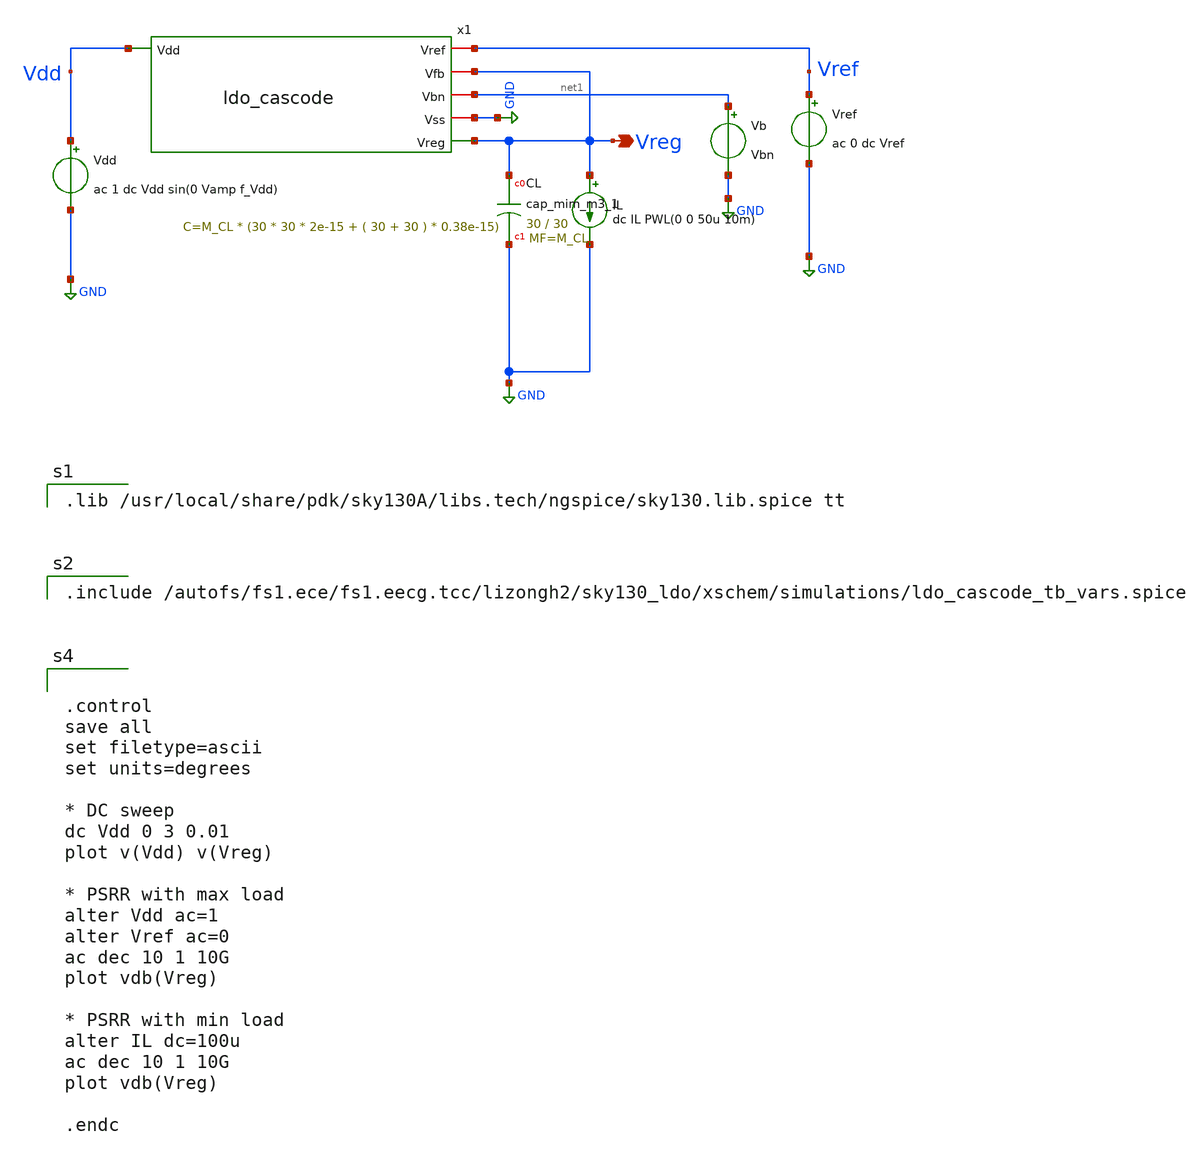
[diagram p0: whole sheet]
** sch_path: xschem/ldo_cascode_tb.sch
**.subckt ldo_cascode_tb Vreg
*.opin Vreg
Vref Vref GND ac 0 dc Vref
Vb net1 GND Vbn
IL Vreg GND dc IL PWL(0 0 50u 10m)
Vdd Vdd GND ac 1 dc Vdd sin(0 Vamp f_Vdd)
XCL Vreg GND sky130_fd_pr__cap_mim_m3_1 W=30 L=30 MF=M_CL m=M_CL
x1 Vdd Vref Vreg net1 GND Vreg ldo_cascode
**** begin user architecture code

.lib /usr/local/share/pdk/sky130A/libs.tech/ngspice/sky130.lib.spice tt



.control
save all
set filetype=ascii
set units=degrees

* DC sweep
dc Vdd 0 3 0.01
plot v(Vdd) v(Vreg)

* PSRR with max load
alter Vdd ac=1
alter Vref ac=0
ac dec 10 1 10G
plot vdb(Vreg)

* PSRR with min load
alter IL dc=100u
ac dec 10 1 10G
plot vdb(Vreg)

.endc



.include /autofs/fs1.ece/fs1.eecg.tcc/lizongh2/sky130_ldo/xschem/simulations/ldo_cascode_tb_vars.spice


**** end user architecture code
**.ends

* expanding   symbol:  ldo_cascode.sym # of pins=6
** sym_path: xschem/ldo_cascode.sym
** sch_path: xschem/ldo_cascode.sch
.subckt ldo_cascode Vdd Vref Vfb Vbn Vss Vreg
*.iopin Vbn
*.iopin Vss
*.opin Vreg
*.iopin Vref
*.ipin Vdd
*.iopin Vfb
XM8 Vreg net1 Vdd Vdd sky130_fd_pr__pfet_g5v0d10v5 L=L_pass W=W_pass nf=1 ad='int((nf+1)/2) * W/nf * 0.29'
+ as='int((nf+2)/2) * W/nf * 0.29' pd='2*int((nf+1)/2) * (W/nf + 0.29)' ps='2*int((nf+2)/2) * (W/nf + 0.29)'
+ nrd='0.29 / W' nrs='0.29 / W' sa=0 sb=0 sd=0 mult=M_pass m=M_pass
Rfb net1 net2 Rfb m=1
Cfb net2 Vreg Cfb m=1
x1 Vdd net1 Vref Vfb Vbn Vss diff_pair_cascode
.ends


* expanding   symbol:  diff_pair_cascode.sym # of pins=6
** sym_path: xschem/diff_pair_cascode.sym
** sch_path: xschem/diff_pair_cascode.sch
.subckt diff_pair_cascode Vdd vout vinm vinp Vbn Vss
*.ipin vinm
*.ipin vinp
*.iopin Vbn
*.opin vout
*.iopin Vss
*.iopin Vdd
XM1 net1 vinp net4 Vss sky130_fd_pr__nfet_g5v0d10v5 L=L_M1 W=W_M1 nf=1 ad='int((nf+1)/2) * W/nf * 0.29'
+ as='int((nf+2)/2) * W/nf * 0.29' pd='2*int((nf+1)/2) * (W/nf + 0.29)' ps='2*int((nf+2)/2) * (W/nf + 0.29)'
+ nrd='0.29 / W' nrs='0.29 / W' sa=0 sb=0 sd=0 mult=1 m=1
XM2 vout vinm net4 Vss sky130_fd_pr__nfet_g5v0d10v5 L=L_M2 W=W_M2 nf=1 ad='int((nf+1)/2) * W/nf * 0.29'
+ as='int((nf+2)/2) * W/nf * 0.29' pd='2*int((nf+1)/2) * (W/nf + 0.29)' ps='2*int((nf+2)/2) * (W/nf + 0.29)'
+ nrd='0.29 / W' nrs='0.29 / W' sa=0 sb=0 sd=0 mult=1 m=1
XM3 vout net1 net3 Vdd sky130_fd_pr__pfet_g5v0d10v5 L=L_M3 W=W_M3 nf=1 ad='int((nf+1)/2) * W/nf * 0.29'
+ as='int((nf+2)/2) * W/nf * 0.29' pd='2*int((nf+1)/2) * (W/nf + 0.29)' ps='2*int((nf+2)/2) * (W/nf + 0.29)'
+ nrd='0.29 / W' nrs='0.29 / W' sa=0 sb=0 sd=0 mult=1 m=1
XM4 net1 net1 net2 Vdd sky130_fd_pr__pfet_g5v0d10v5 L=L_M4 W=W_M4 nf=1 ad='int((nf+1)/2) * W/nf * 0.29'
+ as='int((nf+2)/2) * W/nf * 0.29' pd='2*int((nf+1)/2) * (W/nf + 0.29)' ps='2*int((nf+2)/2) * (W/nf + 0.29)'
+ nrd='0.29 / W' nrs='0.29 / W' sa=0 sb=0 sd=0 mult=1 m=1
XM7 net4 Vbn Vss Vss sky130_fd_pr__nfet_g5v0d10v5 L=L_M7 W=W_M7 nf=1 ad='int((nf+1)/2) * W/nf * 0.29'
+ as='int((nf+2)/2) * W/nf * 0.29' pd='2*int((nf+1)/2) * (W/nf + 0.29)' ps='2*int((nf+2)/2) * (W/nf + 0.29)'
+ nrd='0.29 / W' nrs='0.29 / W' sa=0 sb=0 sd=0 mult=1 m=1
XM5 net3 net2 Vdd Vdd sky130_fd_pr__pfet_g5v0d10v5 L=L_M5 W=W_M5 nf=1 ad='int((nf+1)/2) * W/nf * 0.29'
+ as='int((nf+2)/2) * W/nf * 0.29' pd='2*int((nf+1)/2) * (W/nf + 0.29)' ps='2*int((nf+2)/2) * (W/nf + 0.29)'
+ nrd='0.29 / W' nrs='0.29 / W' sa=0 sb=0 sd=0 mult=1 m=1
XM6 net2 net2 Vdd Vdd sky130_fd_pr__pfet_g5v0d10v5 L=L_M6 W=W_M6 nf=1 ad='int((nf+1)/2) * W/nf * 0.29'
+ as='int((nf+2)/2) * W/nf * 0.29' pd='2*int((nf+1)/2) * (W/nf + 0.29)' ps='2*int((nf+2)/2) * (W/nf + 0.29)'
+ nrd='0.29 / W' nrs='0.29 / W' sa=0 sb=0 sd=0 mult=1 m=1
.ends

.GLOBAL GND
.end
